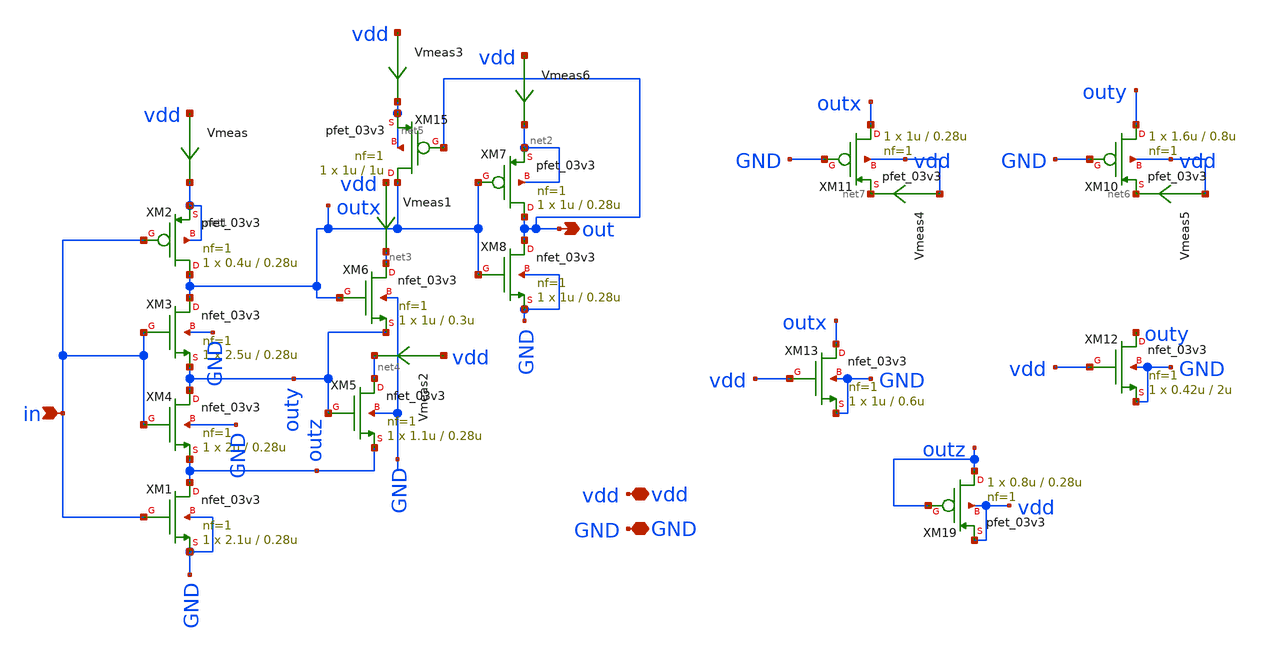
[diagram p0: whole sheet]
** sch_path: designs/libs/core_schmitt_trigger/schmitt_trigger.sch
**.subckt schmitt_trigger in out vdd GND
*.ipin in
*.opin out
*.iopin vdd
*.iopin GND
XM2 outx in net1 net1 pfet_03v3 L=0.28u W=0.4u nf=1 ad='int((nf+1)/2) * W/nf * 0.18u' as='int((nf+2)/2) * W/nf * 0.18u'
+ pd='2*int((nf+1)/2) * (W/nf + 0.18u)' ps='2*int((nf+2)/2) * (W/nf + 0.18u)' nrd='0.18u / W' nrs='0.18u / W'
+ sa=0 sb=0 sd=0 m=1
XM1 outz in GND GND nfet_03v3 L=0.28u W=2.1u nf=1 ad='int((nf+1)/2) * W/nf * 0.18u' as='int((nf+2)/2) * W/nf * 0.18u'
+ pd='2*int((nf+1)/2) * (W/nf + 0.18u)' ps='2*int((nf+2)/2) * (W/nf + 0.18u)' nrd='0.18u / W' nrs='0.18u / W'
+ sa=0 sb=0 sd=0 m=1
XM4 outy in outz GND nfet_03v3 L=0.28u W=2u nf=1 ad='int((nf+1)/2) * W/nf * 0.18u' as='int((nf+2)/2) * W/nf * 0.18u'
+ pd='2*int((nf+1)/2) * (W/nf + 0.18u)' ps='2*int((nf+2)/2) * (W/nf + 0.18u)' nrd='0.18u / W' nrs='0.18u / W'
+ sa=0 sb=0 sd=0 m=1
XM3 outx in outy GND nfet_03v3 L=0.28u W=2.5u nf=1 ad='int((nf+1)/2) * W/nf * 0.18u' as='int((nf+2)/2) * W/nf * 0.18u'
+ pd='2*int((nf+1)/2) * (W/nf + 0.18u)' ps='2*int((nf+2)/2) * (W/nf + 0.18u)' nrd='0.18u / W' nrs='0.18u / W'
+ sa=0 sb=0 sd=0 m=1
XM5 net4 outy outz GND nfet_03v3 L=0.28u W=1.1u nf=1 ad='int((nf+1)/2) * W/nf * 0.18u' as='int((nf+2)/2) * W/nf * 0.18u'
+ pd='2*int((nf+1)/2) * (W/nf + 0.18u)' ps='2*int((nf+2)/2) * (W/nf + 0.18u)' nrd='0.18u / W' nrs='0.18u / W'
+ sa=0 sb=0 sd=0 m=1
XM6 net3 outx outy GND nfet_03v3 L=0.3u W=1u nf=1 ad='int((nf+1)/2) * W/nf * 0.18u' as='int((nf+2)/2) * W/nf * 0.18u'
+ pd='2*int((nf+1)/2) * (W/nf + 0.18u)' ps='2*int((nf+2)/2) * (W/nf + 0.18u)' nrd='0.18u / W' nrs='0.18u / W'
+ sa=0 sb=0 sd=0 m=1
XM8 out outx GND GND nfet_03v3 L=0.28u W=1u nf=1 ad='int((nf+1)/2) * W/nf * 0.18u' as='int((nf+2)/2) * W/nf * 0.18u'
+ pd='2*int((nf+1)/2) * (W/nf + 0.18u)' ps='2*int((nf+2)/2) * (W/nf + 0.18u)' nrd='0.18u / W' nrs='0.18u / W'
+ sa=0 sb=0 sd=0 m=1
XM7 out outx net2 net2 pfet_03v3 L=0.28u W=1u nf=1 ad='int((nf+1)/2) * W/nf * 0.18u' as='int((nf+2)/2) * W/nf * 0.18u'
+ pd='2*int((nf+1)/2) * (W/nf + 0.18u)' ps='2*int((nf+2)/2) * (W/nf + 0.18u)' nrd='0.18u / W' nrs='0.18u / W'
+ sa=0 sb=0 sd=0 m=1
XM10 outy GND net6 vdd pfet_03v3 L=0.8u W=1.6u nf=1 ad='int((nf+1)/2) * W/nf * 0.18u' as='int((nf+2)/2) * W/nf * 0.18u'
+ pd='2*int((nf+1)/2) * (W/nf + 0.18u)' ps='2*int((nf+2)/2) * (W/nf + 0.18u)' nrd='0.18u / W' nrs='0.18u / W'
+ sa=0 sb=0 sd=0 m=1
XM11 outx GND net7 vdd pfet_03v3 L=0.28u W=1u nf=1 ad='int((nf+1)/2) * W/nf * 0.18u' as='int((nf+2)/2) * W/nf * 0.18u'
+ pd='2*int((nf+1)/2) * (W/nf + 0.18u)' ps='2*int((nf+2)/2) * (W/nf + 0.18u)' nrd='0.18u / W' nrs='0.18u / W'
+ sa=0 sb=0 sd=0 m=1
XM12 outy vdd GND GND nfet_03v3 L=2u W=0.42u nf=1 ad='int((nf+1)/2) * W/nf * 0.18u' as='int((nf+2)/2) * W/nf * 0.18u'
+ pd='2*int((nf+1)/2) * (W/nf + 0.18u)' ps='2*int((nf+2)/2) * (W/nf + 0.18u)' nrd='0.18u / W' nrs='0.18u / W'
+ sa=0 sb=0 sd=0 m=1
XM13 outx vdd GND GND nfet_03v3 L=0.6u W=1u nf=1 ad='int((nf+1)/2) * W/nf * 0.18u' as='int((nf+2)/2) * W/nf * 0.18u'
+ pd='2*int((nf+1)/2) * (W/nf + 0.18u)' ps='2*int((nf+2)/2) * (W/nf + 0.18u)' nrd='0.18u / W' nrs='0.18u / W'
+ sa=0 sb=0 sd=0 m=1
XM19 outz outz vdd vdd pfet_03v3 L=0.28u W=0.8u nf=1 ad='int((nf+1)/2) * W/nf * 0.18u' as='int((nf+2)/2) * W/nf * 0.18u'
+ pd='2*int((nf+1)/2) * (W/nf + 0.18u)' ps='2*int((nf+2)/2) * (W/nf + 0.18u)' nrd='0.18u / W' nrs='0.18u / W'
+ sa=0 sb=0 sd=0 m=1
XM15 outx out net5 net5 pfet_03v3 L=1u W=1u nf=1 ad='int((nf+1)/2) * W/nf * 0.18u' as='int((nf+2)/2) * W/nf * 0.18u'
+ pd='2*int((nf+1)/2) * (W/nf + 0.18u)' ps='2*int((nf+2)/2) * (W/nf + 0.18u)' nrd='0.18u / W' nrs='0.18u / W'
+ sa=0 sb=0 sd=0 m=1
Vmeas vdd net1 0
.save i(vmeas)
Vmeas1 vdd net3 0
.save i(vmeas1)
Vmeas2 vdd net4 0
.save i(vmeas2)
Vmeas3 vdd net5 0
.save i(vmeas3)
Vmeas4 vdd net7 0
.save i(vmeas4)
Vmeas5 vdd net6 0
.save i(vmeas5)
Vmeas6 vdd net2 0
.save i(vmeas6)
**.ends
.end
